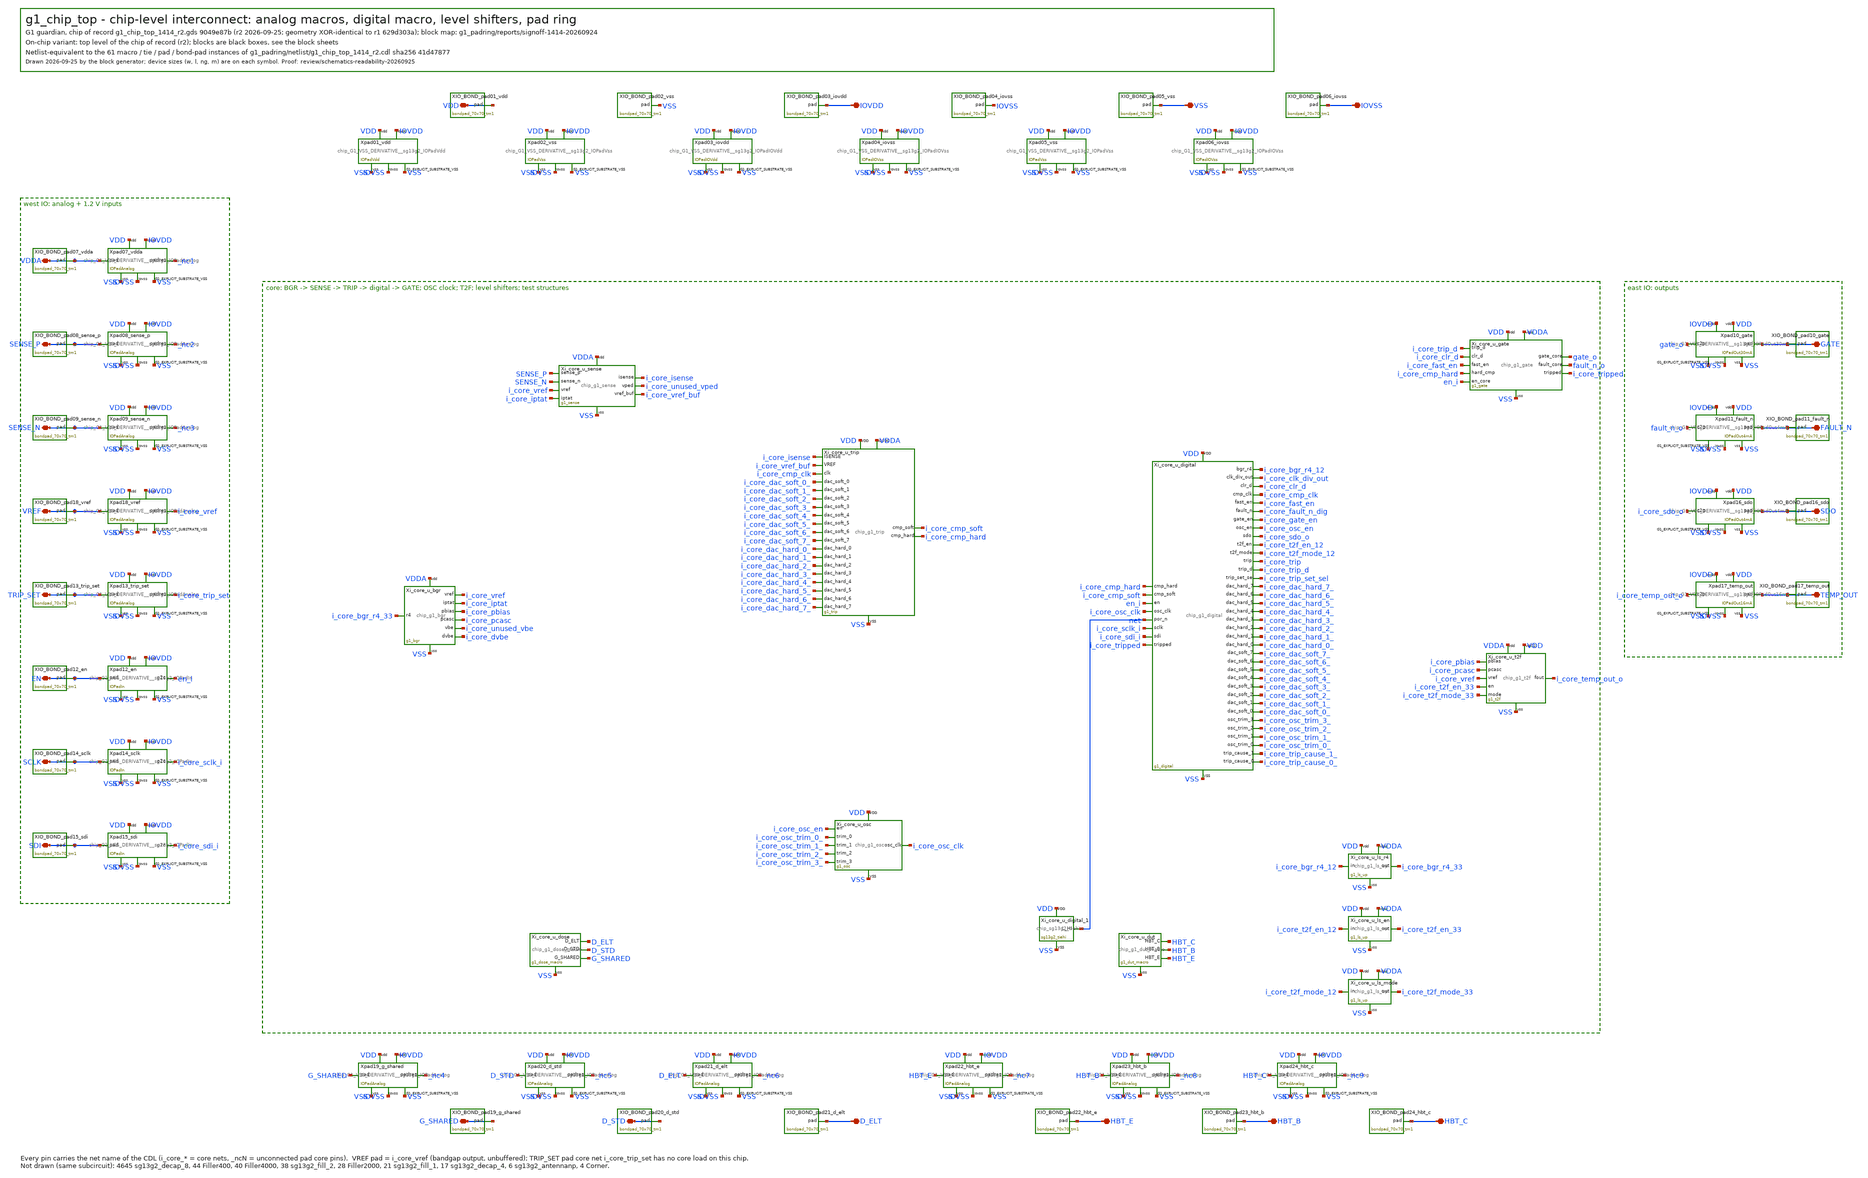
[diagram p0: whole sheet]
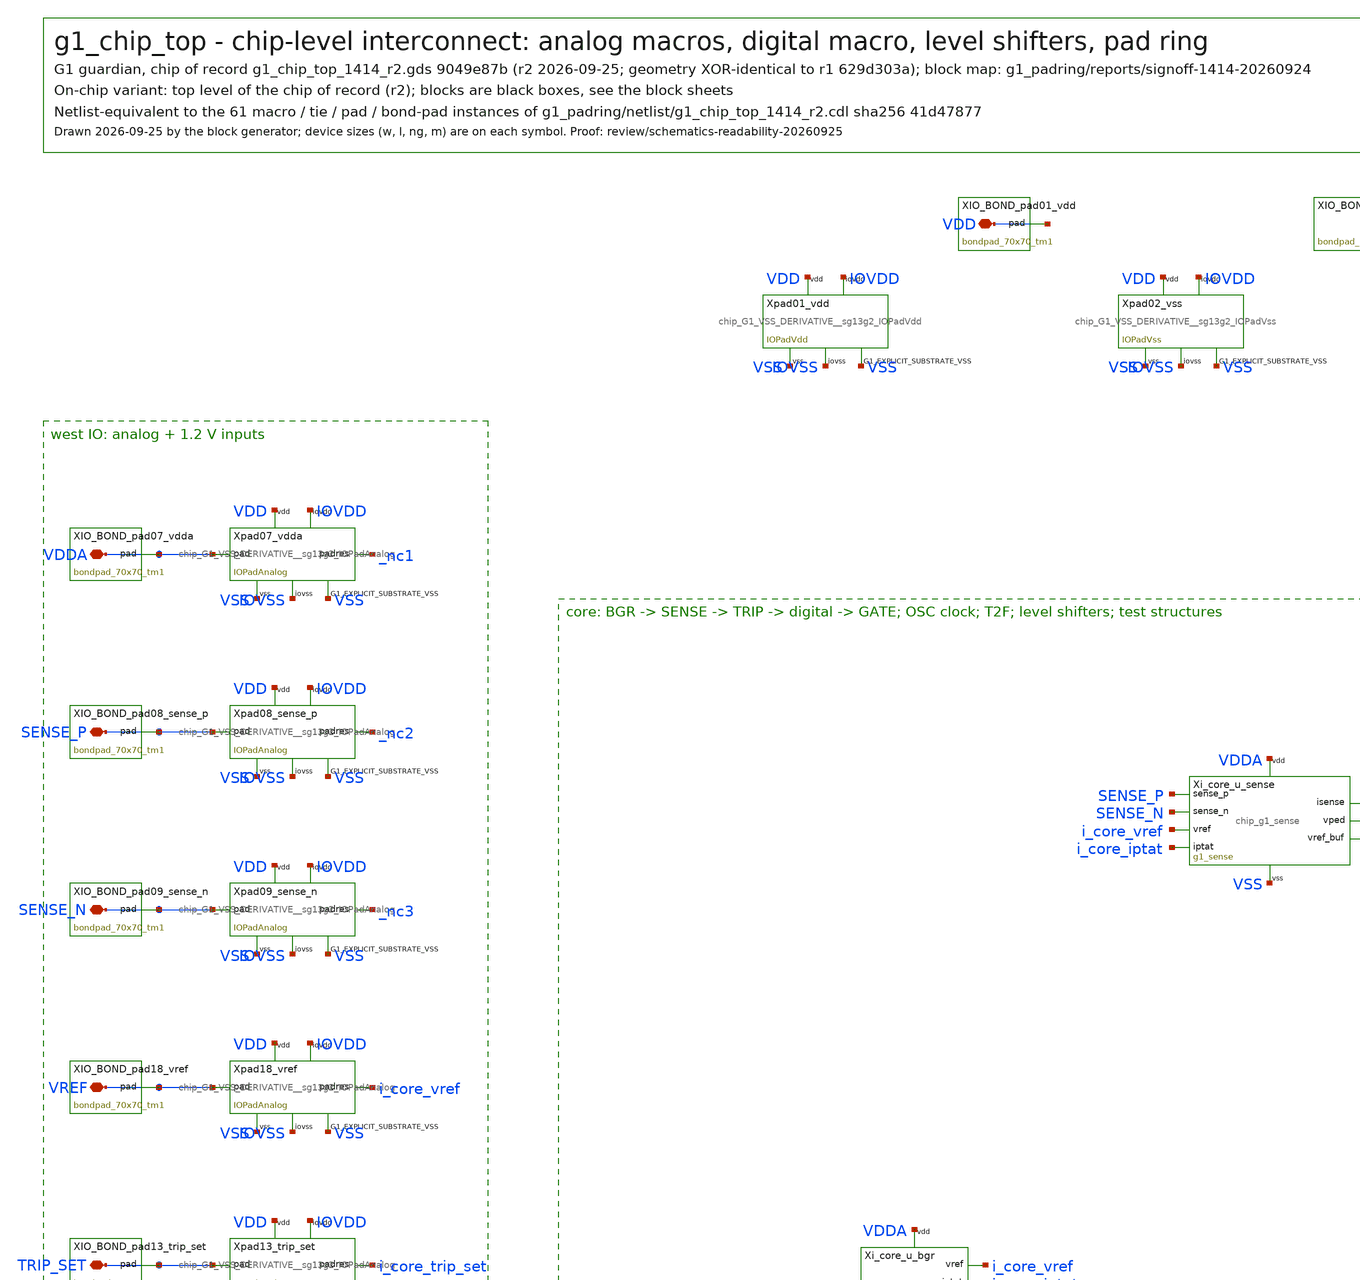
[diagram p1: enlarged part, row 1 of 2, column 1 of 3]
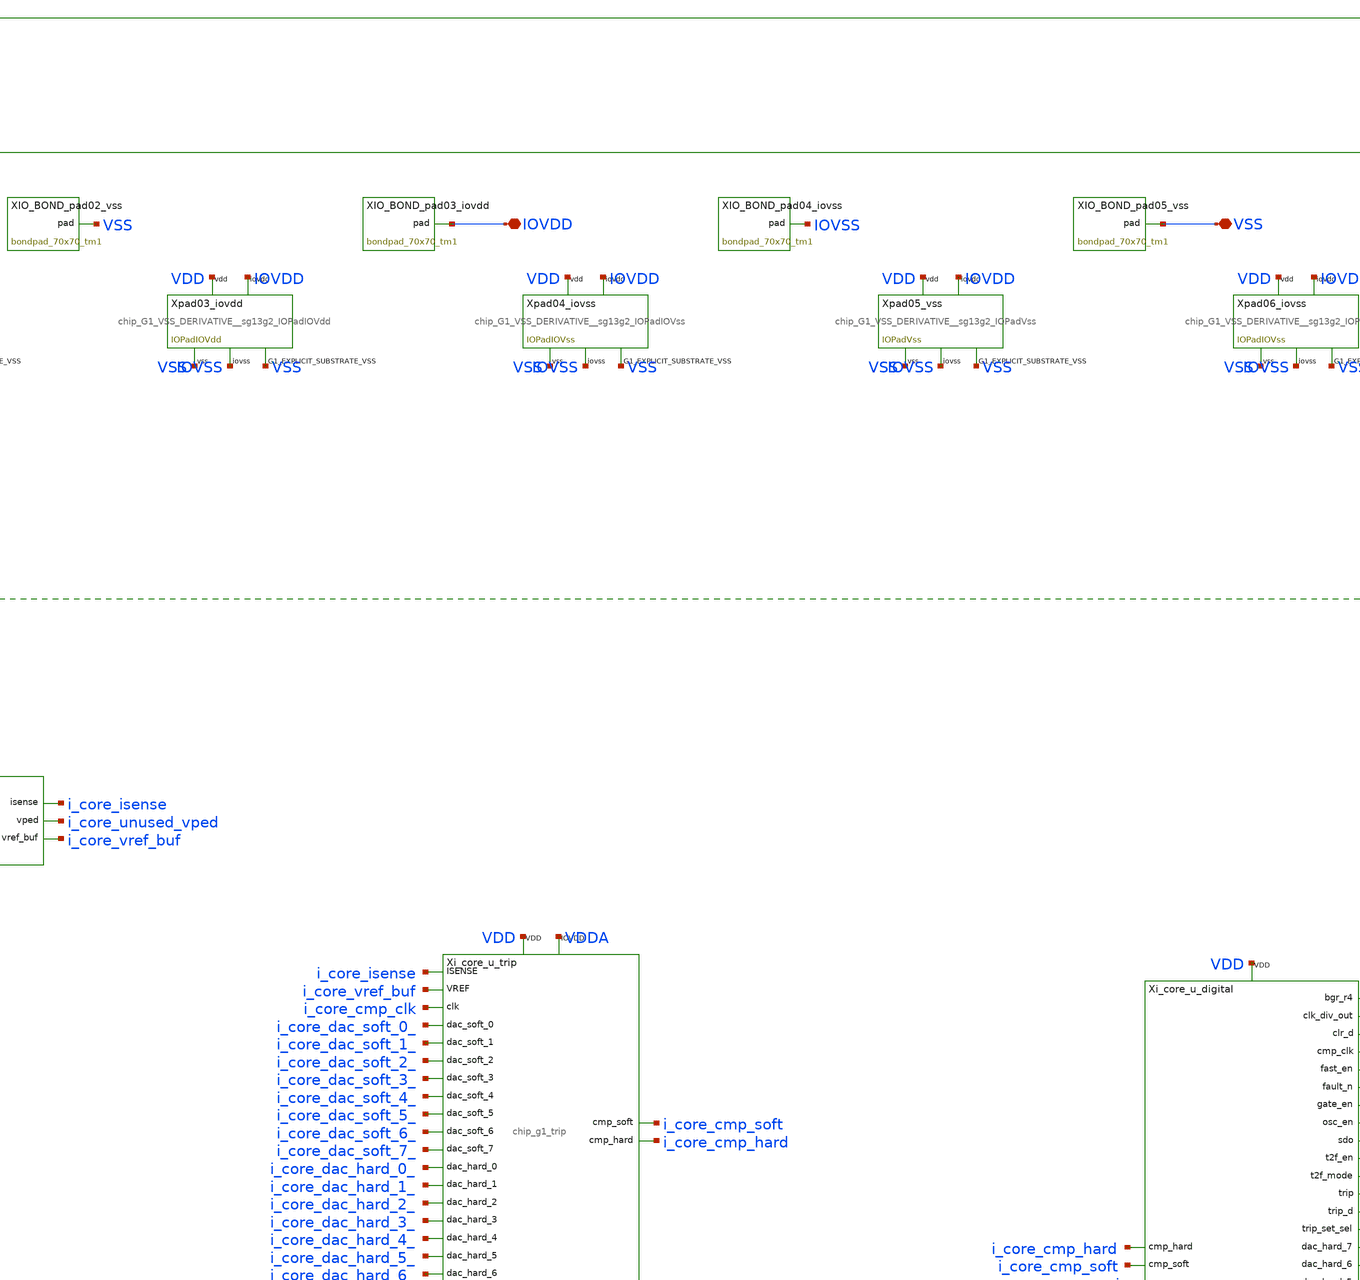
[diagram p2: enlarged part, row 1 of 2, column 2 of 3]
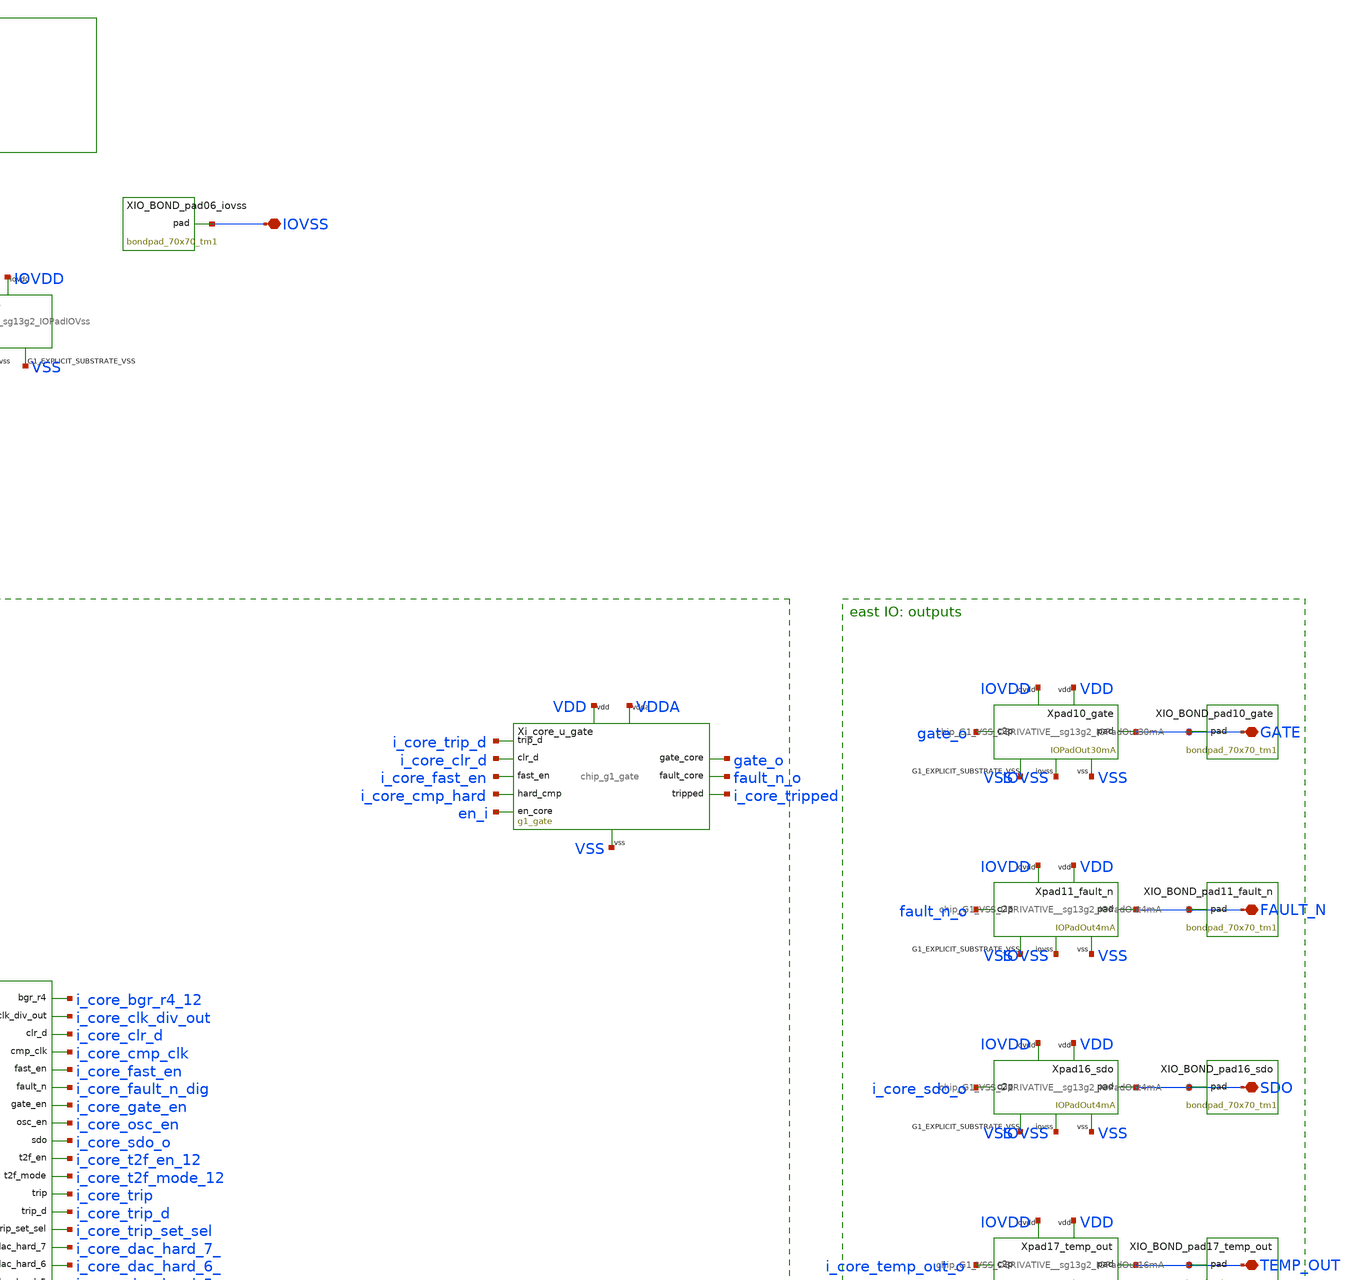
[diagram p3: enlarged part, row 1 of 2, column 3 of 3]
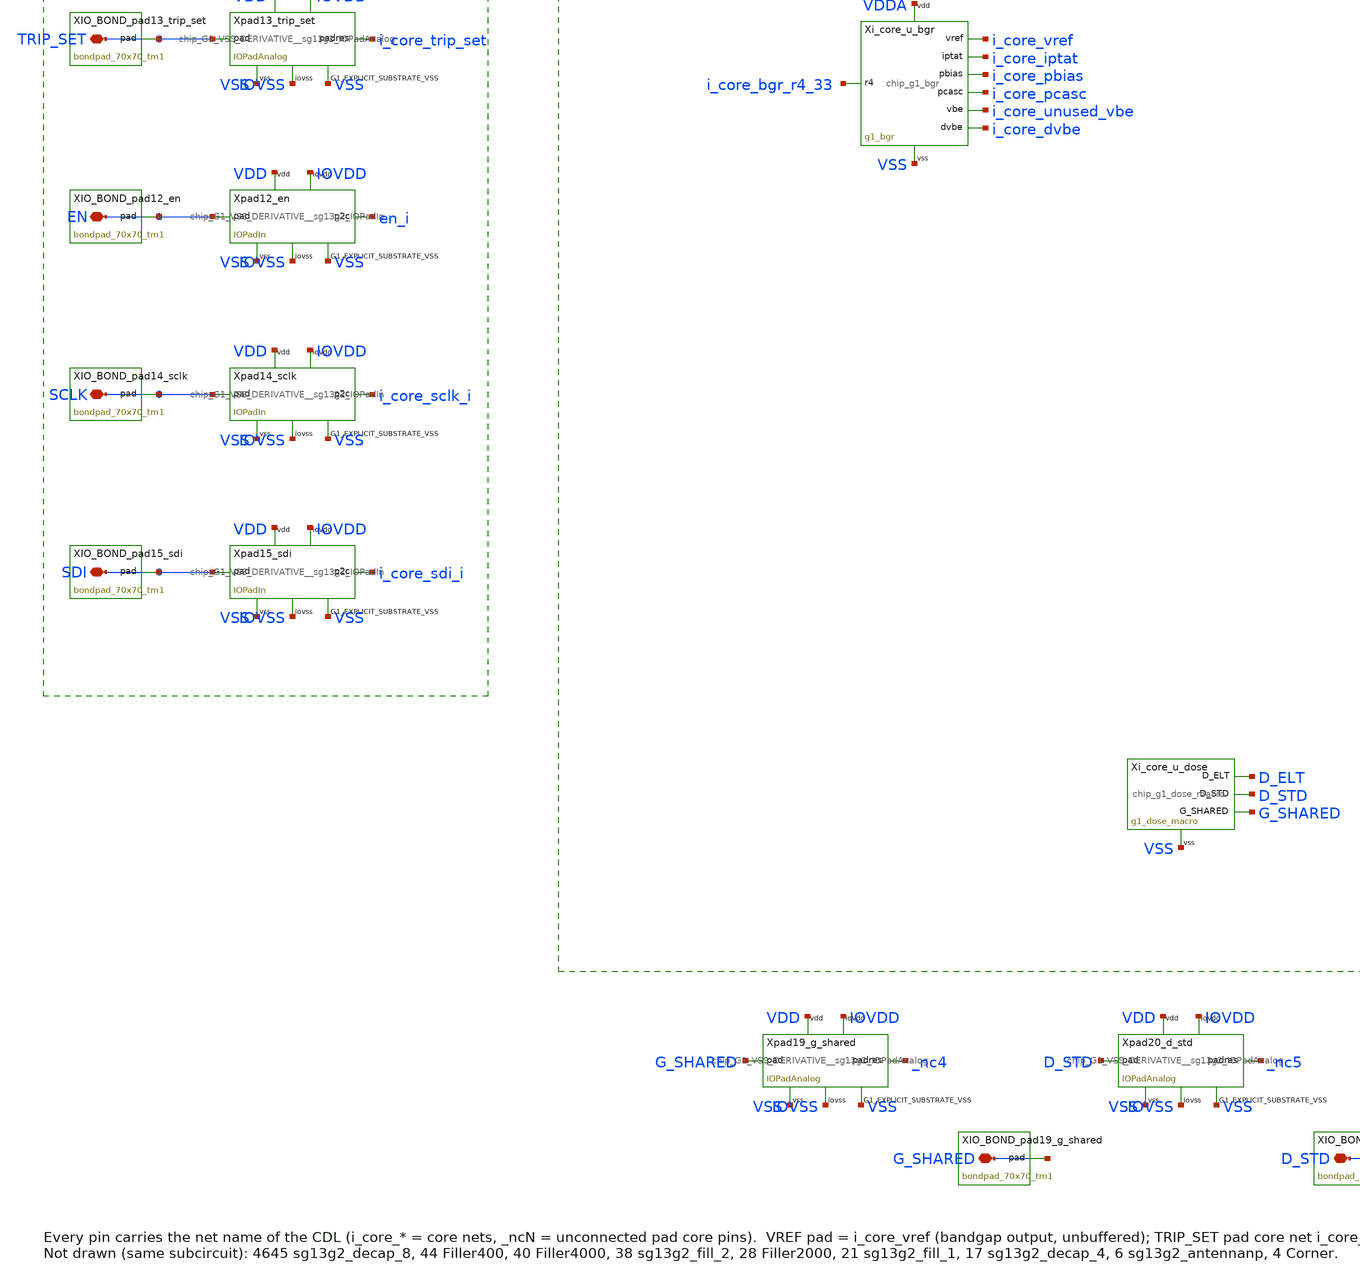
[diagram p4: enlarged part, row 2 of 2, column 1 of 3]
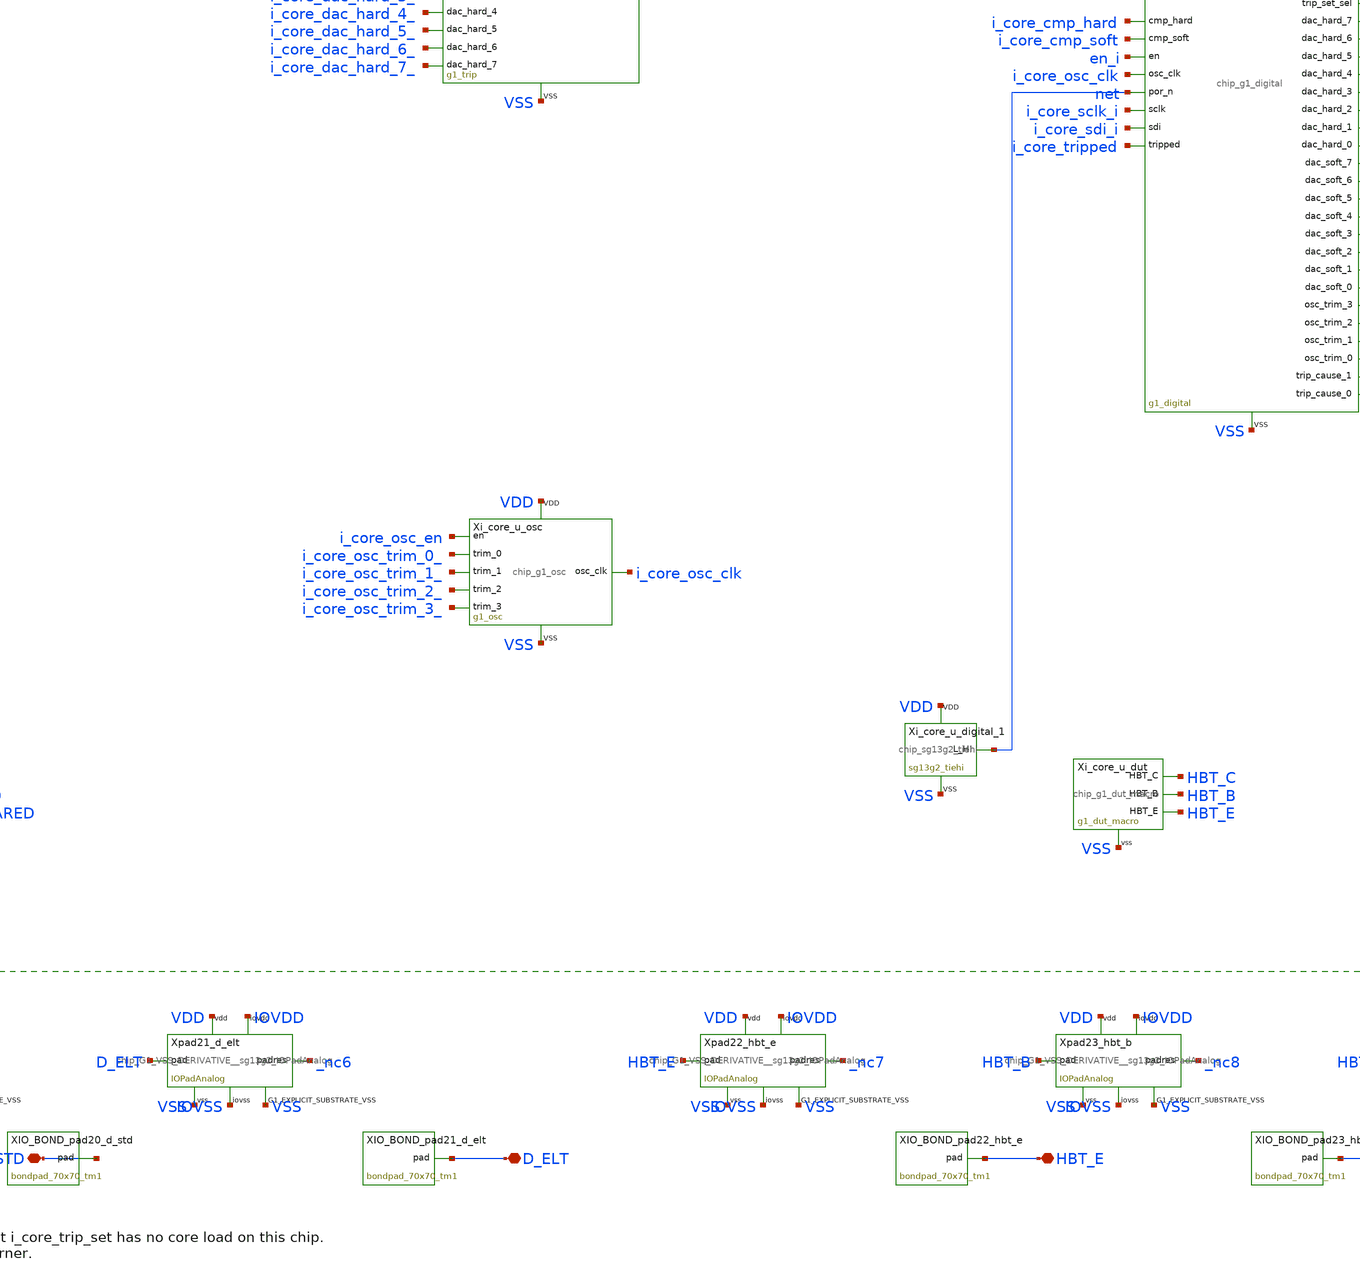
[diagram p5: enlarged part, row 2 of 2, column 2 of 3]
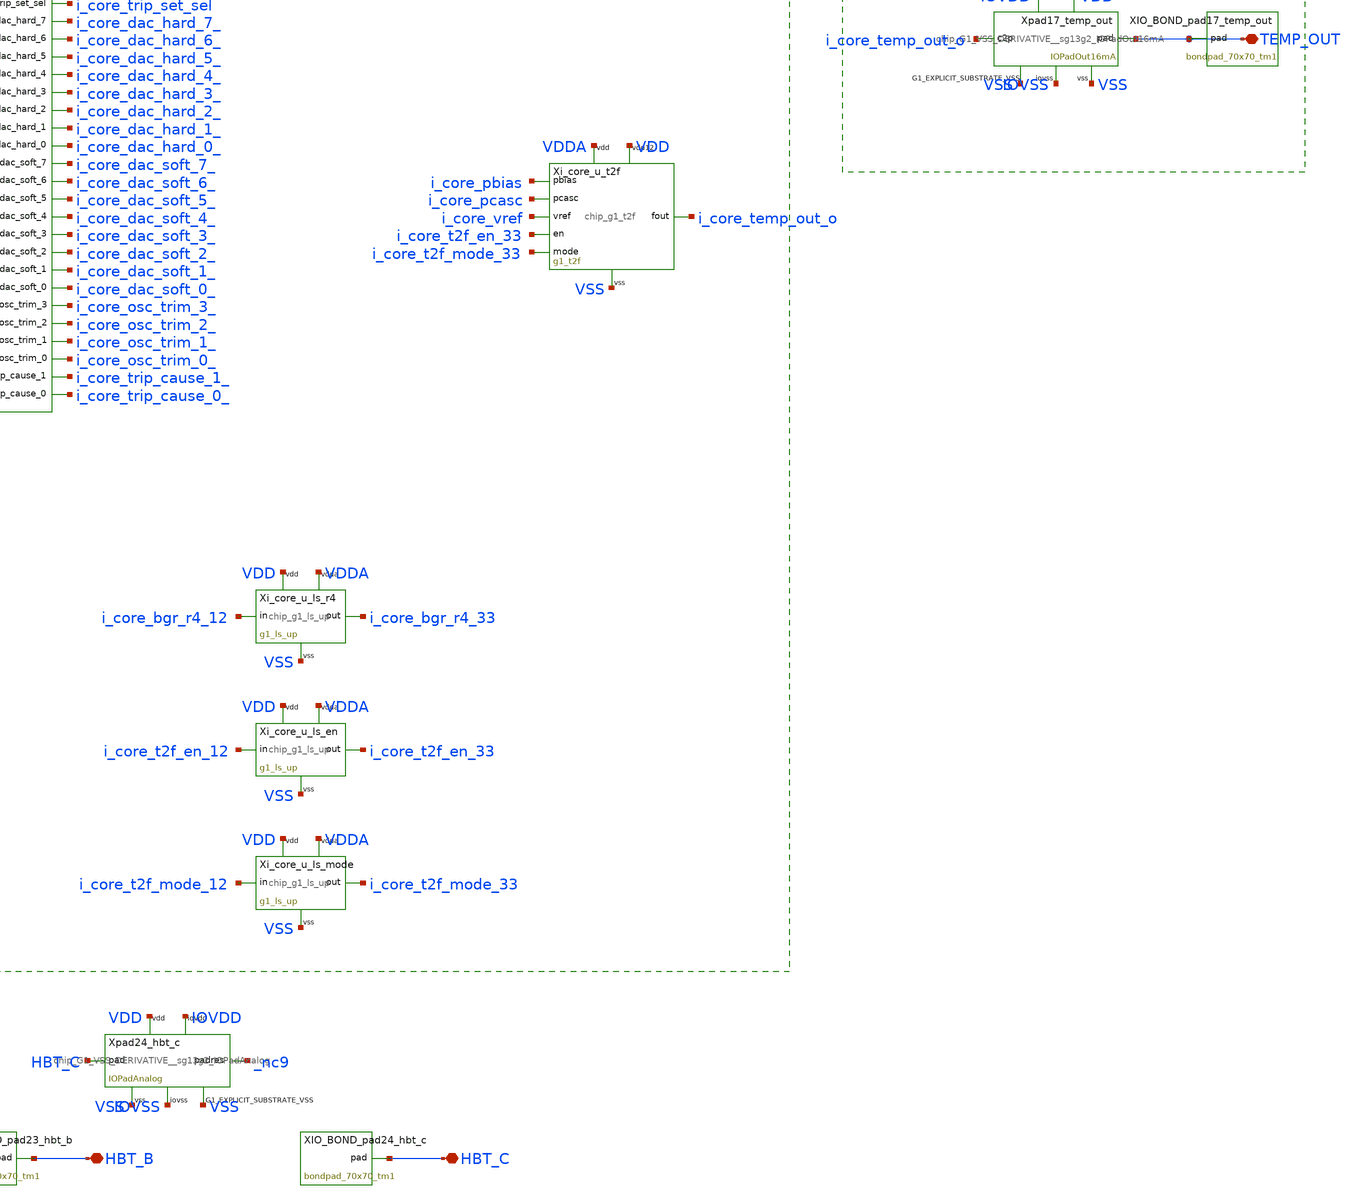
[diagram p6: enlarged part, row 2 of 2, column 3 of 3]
** sch_path: designs/g1-guardian/blocks/g1_top/xschem/chip_interconnect/g1_chip_top.sch
**.subckt g1_chip_top D_ELT D_STD EN FAULT_N GATE G_SHARED HBT_B HBT_C HBT_E SCLK SDI SDO SENSE_N
*+ SENSE_P TEMP_OUT TRIP_SET VDDA VREF VDD VSS IOVDD IOVSS
*.iopin D_ELT
*.iopin D_STD
*.iopin EN
*.iopin FAULT_N
*.iopin GATE
*.iopin G_SHARED
*.iopin HBT_B
*.iopin HBT_C
*.iopin HBT_E
*.iopin SCLK
*.iopin SDI
*.iopin SDO
*.iopin SENSE_N
*.iopin SENSE_P
*.iopin TEMP_OUT
*.iopin TRIP_SET
*.iopin VDDA
*.iopin VREF
*.iopin VDD
*.iopin VSS
*.iopin IOVDD
*.iopin IOVSS
Xi_core_u_bgr VDDA VSS i_core_bgr_r4_33 i_core_vref i_core_iptat i_core_pbias i_core_pcasc
+ i_core_unused_vbe i_core_dvbe g1_bgr
Xi_core_u_digital i_core_bgr_r4_12 i_core_clk_div_out i_core_clr_d i_core_cmp_clk i_core_cmp_hard
+ i_core_cmp_soft en_i i_core_fast_en i_core_fault_n_dig i_core_gate_en i_core_osc_clk i_core_osc_en net
+ i_core_sclk_i i_core_sdi_i i_core_sdo_o i_core_t2f_en_12 i_core_t2f_mode_12 i_core_trip i_core_trip_d
+ i_core_trip_set_sel i_core_tripped VDD VSS i_core_dac_hard_7_ i_core_dac_hard_6_ i_core_dac_hard_5_ i_core_dac_hard_4_
+ i_core_dac_hard_3_ i_core_dac_hard_2_ i_core_dac_hard_1_ i_core_dac_hard_0_ i_core_dac_soft_7_ i_core_dac_soft_6_
+ i_core_dac_soft_5_ i_core_dac_soft_4_ i_core_dac_soft_3_ i_core_dac_soft_2_ i_core_dac_soft_1_ i_core_dac_soft_0_
+ i_core_osc_trim_3_ i_core_osc_trim_2_ i_core_osc_trim_1_ i_core_osc_trim_0_ i_core_trip_cause_1_ i_core_trip_cause_0_
+ g1_digital
Xi_core_u_digital_1 net VDD VSS sg13g2_tiehi
Xi_core_u_dose D_ELT D_STD G_SHARED VSS g1_dose_macro
Xi_core_u_dut HBT_C HBT_B HBT_E VSS g1_dut_macro
Xi_core_u_gate i_core_trip_d i_core_clr_d i_core_fast_en i_core_cmp_hard en_i gate_o fault_n_o
+ i_core_tripped VDD VDDA VSS g1_gate
Xi_core_u_ls_en i_core_t2f_en_12 i_core_t2f_en_33 VDD VDDA VSS g1_ls_up
Xi_core_u_ls_mode i_core_t2f_mode_12 i_core_t2f_mode_33 VDD VDDA VSS g1_ls_up
Xi_core_u_ls_r4 i_core_bgr_r4_12 i_core_bgr_r4_33 VDD VDDA VSS g1_ls_up
Xi_core_u_osc i_core_osc_en i_core_osc_trim_0_ i_core_osc_trim_1_ i_core_osc_trim_2_
+ i_core_osc_trim_3_ i_core_osc_clk VDD VSS g1_osc
Xi_core_u_sense SENSE_P SENSE_N i_core_vref i_core_iptat i_core_isense i_core_unused_vped
+ i_core_vref_buf VDDA VSS g1_sense
Xi_core_u_t2f VDDA VDD VSS i_core_pbias i_core_pcasc i_core_vref i_core_t2f_en_33 i_core_t2f_mode_33
+ i_core_temp_out_o g1_t2f
Xi_core_u_trip i_core_isense i_core_vref_buf i_core_cmp_clk i_core_dac_soft_0_ i_core_dac_soft_1_
+ i_core_dac_soft_2_ i_core_dac_soft_3_ i_core_dac_soft_4_ i_core_dac_soft_5_ i_core_dac_soft_6_ i_core_dac_soft_7_
+ i_core_dac_hard_0_ i_core_dac_hard_1_ i_core_dac_hard_2_ i_core_dac_hard_3_ i_core_dac_hard_4_ i_core_dac_hard_5_
+ i_core_dac_hard_6_ i_core_dac_hard_7_ i_core_cmp_soft i_core_cmp_hard VDD VDDA VSS g1_trip
Xpad01_vdd VDD VSS IOVDD IOVSS VSS G1_VSS_DERIVATIVE__sg13g2_IOPadVdd
Xpad02_vss VDD VSS IOVDD IOVSS VSS G1_VSS_DERIVATIVE__sg13g2_IOPadVss
Xpad03_iovdd VDD VSS IOVDD IOVSS VSS G1_VSS_DERIVATIVE__sg13g2_IOPadIOVdd
Xpad04_iovss VDD VSS IOVDD IOVSS VSS G1_VSS_DERIVATIVE__sg13g2_IOPadIOVss
Xpad05_vss VDD VSS IOVDD IOVSS VSS G1_VSS_DERIVATIVE__sg13g2_IOPadVss
Xpad06_iovss VDD VSS IOVDD IOVSS VSS G1_VSS_DERIVATIVE__sg13g2_IOPadIOVss
Xpad07_vdda VDDA _nc1 VDD VSS IOVDD IOVSS VSS G1_VSS_DERIVATIVE__sg13g2_IOPadAnalog
Xpad08_sense_p SENSE_P _nc2 VDD VSS IOVDD IOVSS VSS G1_VSS_DERIVATIVE__sg13g2_IOPadAnalog
Xpad09_sense_n SENSE_N _nc3 VDD VSS IOVDD IOVSS VSS G1_VSS_DERIVATIVE__sg13g2_IOPadAnalog
Xpad10_gate GATE gate_o VDD VSS IOVDD IOVSS VSS G1_VSS_DERIVATIVE__sg13g2_IOPadOut30mA
Xpad11_fault_n FAULT_N fault_n_o VDD VSS IOVDD IOVSS VSS G1_VSS_DERIVATIVE__sg13g2_IOPadOut4mA
Xpad12_en EN en_i VDD VSS IOVDD IOVSS VSS G1_VSS_DERIVATIVE__sg13g2_IOPadIn
Xpad13_trip_set TRIP_SET i_core_trip_set VDD VSS IOVDD IOVSS VSS
+ G1_VSS_DERIVATIVE__sg13g2_IOPadAnalog
Xpad14_sclk SCLK i_core_sclk_i VDD VSS IOVDD IOVSS VSS G1_VSS_DERIVATIVE__sg13g2_IOPadIn
Xpad15_sdi SDI i_core_sdi_i VDD VSS IOVDD IOVSS VSS G1_VSS_DERIVATIVE__sg13g2_IOPadIn
Xpad16_sdo SDO i_core_sdo_o VDD VSS IOVDD IOVSS VSS G1_VSS_DERIVATIVE__sg13g2_IOPadOut4mA
Xpad17_temp_out TEMP_OUT i_core_temp_out_o VDD VSS IOVDD IOVSS VSS
+ G1_VSS_DERIVATIVE__sg13g2_IOPadOut16mA
Xpad18_vref VREF i_core_vref VDD VSS IOVDD IOVSS VSS G1_VSS_DERIVATIVE__sg13g2_IOPadAnalog
Xpad19_g_shared G_SHARED _nc4 VDD VSS IOVDD IOVSS VSS G1_VSS_DERIVATIVE__sg13g2_IOPadAnalog
Xpad20_d_std D_STD _nc5 VDD VSS IOVDD IOVSS VSS G1_VSS_DERIVATIVE__sg13g2_IOPadAnalog
Xpad21_d_elt D_ELT _nc6 VDD VSS IOVDD IOVSS VSS G1_VSS_DERIVATIVE__sg13g2_IOPadAnalog
Xpad22_hbt_e HBT_E _nc7 VDD VSS IOVDD IOVSS VSS G1_VSS_DERIVATIVE__sg13g2_IOPadAnalog
Xpad23_hbt_b HBT_B _nc8 VDD VSS IOVDD IOVSS VSS G1_VSS_DERIVATIVE__sg13g2_IOPadAnalog
Xpad24_hbt_c HBT_C _nc9 VDD VSS IOVDD IOVSS VSS G1_VSS_DERIVATIVE__sg13g2_IOPadAnalog
XIO_BOND_pad01_vdd VDD bondpad_70x70_tm1
XIO_BOND_pad02_vss VSS bondpad_70x70_tm1
XIO_BOND_pad03_iovdd IOVDD bondpad_70x70_tm1
XIO_BOND_pad04_iovss IOVSS bondpad_70x70_tm1
XIO_BOND_pad05_vss VSS bondpad_70x70_tm1
XIO_BOND_pad06_iovss IOVSS bondpad_70x70_tm1
XIO_BOND_pad07_vdda VDDA bondpad_70x70_tm1
XIO_BOND_pad08_sense_p SENSE_P bondpad_70x70_tm1
XIO_BOND_pad09_sense_n SENSE_N bondpad_70x70_tm1
XIO_BOND_pad10_gate GATE bondpad_70x70_tm1
XIO_BOND_pad11_fault_n FAULT_N bondpad_70x70_tm1
XIO_BOND_pad12_en EN bondpad_70x70_tm1
XIO_BOND_pad13_trip_set TRIP_SET bondpad_70x70_tm1
XIO_BOND_pad14_sclk SCLK bondpad_70x70_tm1
XIO_BOND_pad15_sdi SDI bondpad_70x70_tm1
XIO_BOND_pad16_sdo SDO bondpad_70x70_tm1
XIO_BOND_pad17_temp_out TEMP_OUT bondpad_70x70_tm1
XIO_BOND_pad18_vref VREF bondpad_70x70_tm1
XIO_BOND_pad19_g_shared G_SHARED bondpad_70x70_tm1
XIO_BOND_pad20_d_std D_STD bondpad_70x70_tm1
XIO_BOND_pad21_d_elt D_ELT bondpad_70x70_tm1
XIO_BOND_pad22_hbt_e HBT_E bondpad_70x70_tm1
XIO_BOND_pad23_hbt_b HBT_B bondpad_70x70_tm1
XIO_BOND_pad24_hbt_c HBT_C bondpad_70x70_tm1
**.ends
.end
